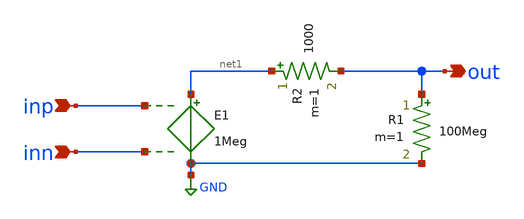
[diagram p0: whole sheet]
** sch_path: DSM_1storder/Schematic_Level/xschem/idealopampa_newspecs.sch
**.subckt idealopampa_newspecs out inp inn
*.opin out
*.ipin inp
*.ipin inn
E1 net1 GND inp inn 1Meg
R1 out GND 100Meg m=1
R2 net1 out 1000 m=1
**.ends
.GLOBAL GND
.end
